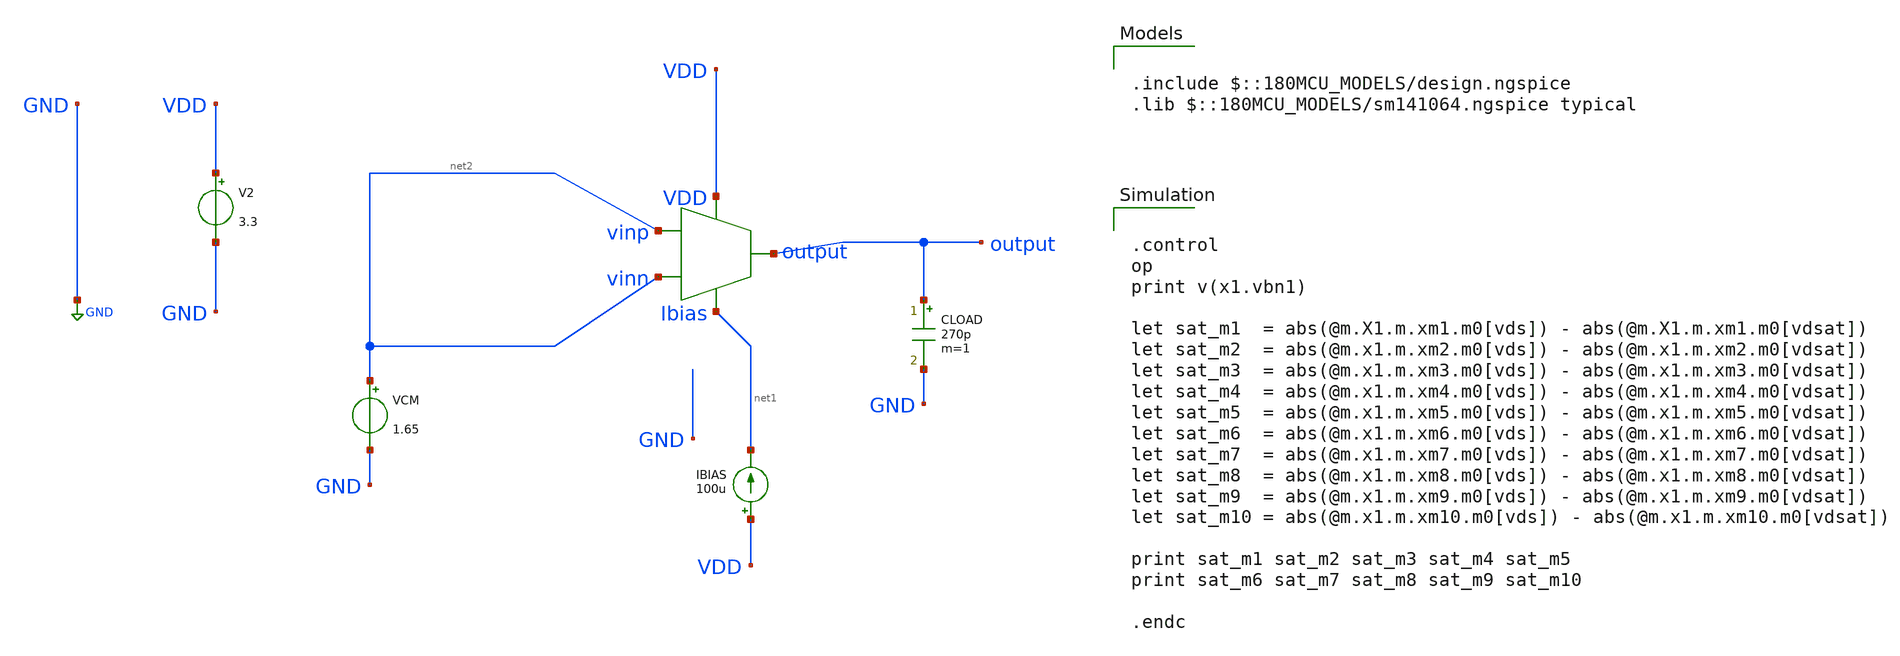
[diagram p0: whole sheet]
** sch_path: designs/libs/core_amps/ota_telescopic/telescopic_vdsat_tb.sch
**.subckt telescopic_vdsat_tb
IBIAS VDD net1 100u
V2 VDD GND 3.3
CLOAD output GND 270p m=1
VCM net2 GND 1.65
X1 net2 net2 VDD net1 output telescopic_cascode
**** begin user architecture code

.include $::180MCU_MODELS/design.ngspice
.lib $::180MCU_MODELS/sm141064.ngspice typical



.control
op
print v(x1.vbn1)

let sat_m1  = abs(@m.X1.m.xm1.m0[vds]) - abs(@m.X1.m.xm1.m0[vdsat])
let sat_m2  = abs(@m.x1.m.xm2.m0[vds]) - abs(@m.x1.m.xm2.m0[vdsat])
let sat_m3  = abs(@m.x1.m.xm3.m0[vds]) - abs(@m.x1.m.xm3.m0[vdsat])
let sat_m4  = abs(@m.x1.m.xm4.m0[vds]) - abs(@m.x1.m.xm4.m0[vdsat])
let sat_m5  = abs(@m.x1.m.xm5.m0[vds]) - abs(@m.x1.m.xm5.m0[vdsat])
let sat_m6  = abs(@m.x1.m.xm6.m0[vds]) - abs(@m.x1.m.xm6.m0[vdsat])
let sat_m7  = abs(@m.x1.m.xm7.m0[vds]) - abs(@m.x1.m.xm7.m0[vdsat])
let sat_m8  = abs(@m.x1.m.xm8.m0[vds]) - abs(@m.x1.m.xm8.m0[vdsat])
let sat_m9  = abs(@m.x1.m.xm9.m0[vds]) - abs(@m.x1.m.xm9.m0[vdsat])
let sat_m10 = abs(@m.x1.m.xm10.m0[vds]) - abs(@m.x1.m.xm10.m0[vdsat])

print sat_m1 sat_m2 sat_m3 sat_m4 sat_m5
print sat_m6 sat_m7 sat_m8 sat_m9 sat_m10

.endc



**** end user architecture code
**.ends

* expanding   symbol:  libs/core_amps/ota_telescopic/telescopic_cascode.sym # of pins=5
** sym_path: designs/libs/core_amps/ota_telescopic/telescopic_cascode.sym
** sch_path: designs/libs/core_amps/ota_telescopic/telescopic_cascode.sch
.subckt telescopic_cascode vinp vinn VDD Ibias output
*.ipin vinp
*.ipin vinn
*.opin output
*.iopin Ibias
*.iopin VDD
XM8 output net4 net3 VDD pfet_03v3 L=0.56u W=65u nf=1 ad='int((nf+1)/2) * W/nf * 0.18u' as='int((nf+2)/2) * W/nf * 0.18u'
+ pd='2*int((nf+1)/2) * (W/nf + 0.18u)' ps='2*int((nf+2)/2) * (W/nf + 0.18u)' nrd='0.18u / W' nrs='0.18u / W'
+ sa=0 sb=0 sd=0 m=4
XM4 output VBN1 net7 GND nfet_03v3 L=0.5u W=40u nf=1 ad='int((nf+1)/2) * W/nf * 0.18u' as='int((nf+2)/2) * W/nf * 0.18u'
+ pd='2*int((nf+1)/2) * (W/nf + 0.18u)' ps='2*int((nf+2)/2) * (W/nf + 0.18u)' nrd='0.18u / W' nrs='0.18u / W'
+ sa=0 sb=0 sd=0 m=1
XM1 net5 vinp net6 GND nfet_03v3 L=0.5u W=30u nf=1 ad='int((nf+1)/2) * W/nf * 0.18u' as='int((nf+2)/2) * W/nf * 0.18u'
+ pd='2*int((nf+1)/2) * (W/nf + 0.18u)' ps='2*int((nf+2)/2) * (W/nf + 0.18u)' nrd='0.18u / W' nrs='0.18u / W'
+ sa=0 sb=0 sd=0 m=1
XM2 net1 VBN1 net5 GND nfet_03v3 L=0.5u W=40u nf=1 ad='int((nf+1)/2) * W/nf * 0.18u' as='int((nf+2)/2) * W/nf * 0.18u'
+ pd='2*int((nf+1)/2) * (W/nf + 0.18u)' ps='2*int((nf+2)/2) * (W/nf + 0.18u)' nrd='0.18u / W' nrs='0.18u / W'
+ sa=0 sb=0 sd=0 m=1
XM3 net7 vinn net6 GND nfet_03v3 L=0.5u W=30u nf=1 ad='int((nf+1)/2) * W/nf * 0.18u' as='int((nf+2)/2) * W/nf * 0.18u'
+ pd='2*int((nf+1)/2) * (W/nf + 0.18u)' ps='2*int((nf+2)/2) * (W/nf + 0.18u)' nrd='0.18u / W' nrs='0.18u / W'
+ sa=0 sb=0 sd=0 m=1
XM5 net3 net1 VDD VDD pfet_03v3 L=0.56u W=65u nf=1 ad='int((nf+1)/2) * W/nf * 0.18u' as='int((nf+2)/2) * W/nf * 0.18u'
+ pd='2*int((nf+1)/2) * (W/nf + 0.18u)' ps='2*int((nf+2)/2) * (W/nf + 0.18u)' nrd='0.18u / W' nrs='0.18u / W'
+ sa=0 sb=0 sd=0 m=4
XM6 net1 net4 net2 VDD pfet_03v3 L=0.56u W=65u nf=1 ad='int((nf+1)/2) * W/nf * 0.18u' as='int((nf+2)/2) * W/nf * 0.18u'
+ pd='2*int((nf+1)/2) * (W/nf + 0.18u)' ps='2*int((nf+2)/2) * (W/nf + 0.18u)' nrd='0.18u / W' nrs='0.18u / W'
+ sa=0 sb=0 sd=0 m=4
XM7 net2 net1 VDD VDD pfet_03v3 L=0.56u W=65u nf=1 ad='int((nf+1)/2) * W/nf * 0.18u' as='int((nf+2)/2) * W/nf * 0.18u'
+ pd='2*int((nf+1)/2) * (W/nf + 0.18u)' ps='2*int((nf+2)/2) * (W/nf + 0.18u)' nrd='0.18u / W' nrs='0.18u / W'
+ sa=0 sb=0 sd=0 m=4
XM9 net6 Ibias GND GND nfet_03v3 L=0.28u W=15.54u nf=1 ad='int((nf+1)/2) * W/nf * 0.18u' as='int((nf+2)/2) * W/nf * 0.18u'
+ pd='2*int((nf+1)/2) * (W/nf + 0.18u)' ps='2*int((nf+2)/2) * (W/nf + 0.18u)' nrd='0.18u / W' nrs='0.18u / W'
+ sa=0 sb=0 sd=0 m=1
XM10 Ibias Ibias GND GND nfet_03v3 L=.28u W=5.18u nf=1 ad='int((nf+1)/2) * W/nf * 0.18u' as='int((nf+2)/2) * W/nf * 0.18u'
+ pd='2*int((nf+1)/2) * (W/nf + 0.18u)' ps='2*int((nf+2)/2) * (W/nf + 0.18u)' nrd='0.18u / W' nrs='0.18u / W'
+ sa=0 sb=0 sd=0 m=1
**** begin user architecture code


.include /foss/pdks/gf180mcuD/libs.tech/ngspice/design.ngspice
.lib /foss/pdks/gf180mcuD/libs.tech/ngspice/sm141064.ngspice typical

**** end user architecture code
V1 VBN1 GND 2.2
V2 net4 GND 1.6
.ends

.GLOBAL GND
.end
